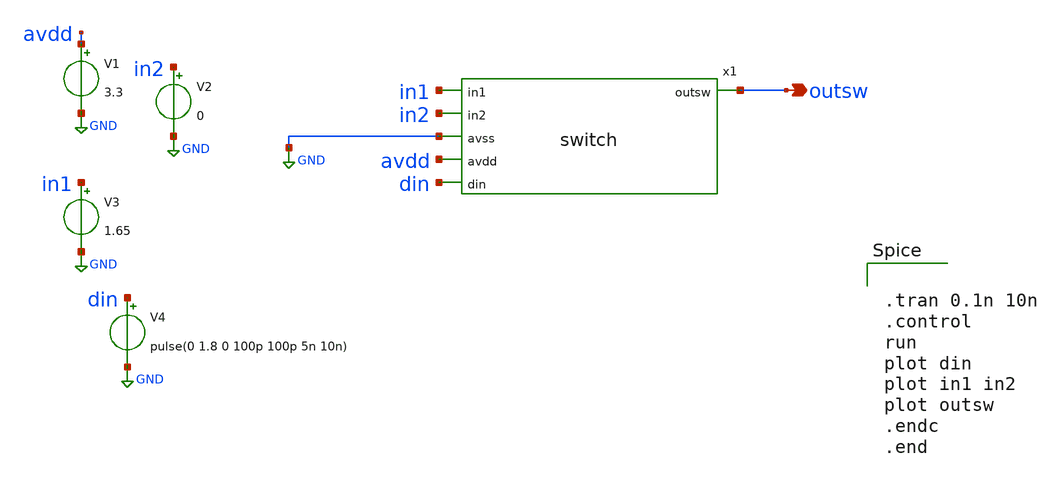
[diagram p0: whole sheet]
** sch_path: xschem/tb_switch.sch
**.subckt tb_switch outsw
*.opin outsw
V1 avdd GND 3.3
V2 in2 GND 0
V3 in1 GND 1.65
V4 din GND pulse(0 1.8 0 100p 100p 5n 10n)
x1 outsw in1 in2 GND avdd din switch
**** begin user architecture code

** opencircuitdesign pdks install
.lib $::SKYWATER_MODELS/sky130.lib.spice tt




.tran 0.1n 10n
.control
run
plot din
plot in1 in2
plot outsw
.endc
.end

**** end user architecture code
**.ends

* expanding   symbol:  switch.sym # of pins=6
** sym_path: xschem/switch.sym
** sch_path: xschem/switch.sch
.subckt switch outsw in1 in2 avss avdd din
*.ipin avss
*.ipin avdd
*.ipin din
*.ipin in1
*.ipin in2
*.opin outsw
XM11 dinbar din avdd avdd sky130_fd_pr__pfet_01v8 L=0.15 W=1.2 nf=1 ad='int((nf+1)/2) * W/nf * 0.29'
+ as='int((nf+2)/2) * W/nf * 0.29' pd='2*int((nf+1)/2) * (W/nf + 0.29)' ps='2*int((nf+2)/2) * (W/nf + 0.29)'
+ nrd='0.29 / W' nrs='0.29 / W' sa=0 sb=0 sd=0 mult=1 m=1
XM1 wc dinbar avdd avdd sky130_fd_pr__pfet_01v8 L=0.15 W=1.2 nf=1 ad='int((nf+1)/2) * W/nf * 0.29' as='int((nf+2)/2) * W/nf * 0.29'
+ pd='2*int((nf+1)/2) * (W/nf + 0.29)' ps='2*int((nf+2)/2) * (W/nf + 0.29)' nrd='0.29 / W' nrs='0.29 / W'
+ sa=0 sb=0 sd=0 mult=1 m=1
XM2 dinbar din avss avss sky130_fd_pr__nfet_01v8 L=0.15 W=0.6 nf=1 ad='int((1 + 1)/2) * 0.6 / 1 * 0.29'
+ as='int((1 + 2)/2) * 0.6 / 1 * 0.29' pd='2*int((1 + 1)/2) * (0.6 / 1 + 0.29)' ps='2*int((1 + 2)/2) * (0.6 / 1 + 0.29)'
+ nrd='0.29 / 0.6 ' nrs='0.29 / 0.6 ' sa=0 sb=0 sd=0 mult=1 m=1
XM3 wc dinbar avss avss sky130_fd_pr__nfet_01v8 L=0.15 W=0.6 nf=1 ad='int((1 + 1)/2) * 0.6 / 1 * 0.29'
+ as='int((1 + 2)/2) * 0.6 / 1 * 0.29' pd='2*int((1 + 1)/2) * (0.6 / 1 + 0.29)' ps='2*int((1 + 2)/2) * (0.6 / 1 + 0.29)'
+ nrd='0.29 / 0.6 ' nrs='0.29 / 0.6 ' sa=0 sb=0 sd=0 mult=1 m=1
XM4 outsw dinbar in1 avdd sky130_fd_pr__pfet_01v8 L=0.15 W=1.2 nf=1 ad='int((nf+1)/2) * W/nf * 0.29'
+ as='int((nf+2)/2) * W/nf * 0.29' pd='2*int((nf+1)/2) * (W/nf + 0.29)' ps='2*int((nf+2)/2) * (W/nf + 0.29)'
+ nrd='0.29 / W' nrs='0.29 / W' sa=0 sb=0 sd=0 mult=1 m=1
XM5 outsw dinbar in2 avss sky130_fd_pr__nfet_01v8 L=0.15 W=0.6 nf=1 ad='int((1 + 1)/2) * 0.6 / 1 * 0.29'
+ as='int((1 + 2)/2) * 0.6 / 1 * 0.29' pd='2*int((1 + 1)/2) * (0.6 / 1 + 0.29)' ps='2*int((1 + 2)/2) * (0.6 / 1 + 0.29)'
+ nrd='0.29 / 0.6 ' nrs='0.29 / 0.6 ' sa=0 sb=0 sd=0 mult=1 m=1
XM6 in1 wc outsw avss sky130_fd_pr__nfet_01v8 L=0.15 W=0.6 nf=1 ad='int((1 + 1)/2) * 0.6 / 1 * 0.29'
+ as='int((1 + 2)/2) * 0.6 / 1 * 0.29' pd='2*int((1 + 1)/2) * (0.6 / 1 + 0.29)' ps='2*int((1 + 2)/2) * (0.6 / 1 + 0.29)'
+ nrd='0.29 / 0.6 ' nrs='0.29 / 0.6 ' sa=0 sb=0 sd=0 mult=1 m=1
XM7 in2 wc outsw avdd sky130_fd_pr__pfet_01v8 L=0.15 W=1.2 nf=1 ad='int((nf+1)/2) * W/nf * 0.29' as='int((nf+2)/2) * W/nf * 0.29'
+ pd='2*int((nf+1)/2) * (W/nf + 0.29)' ps='2*int((nf+2)/2) * (W/nf + 0.29)' nrd='0.29 / W' nrs='0.29 / W'
+ sa=0 sb=0 sd=0 mult=1 m=1
.ends

.GLOBAL GND
.end
